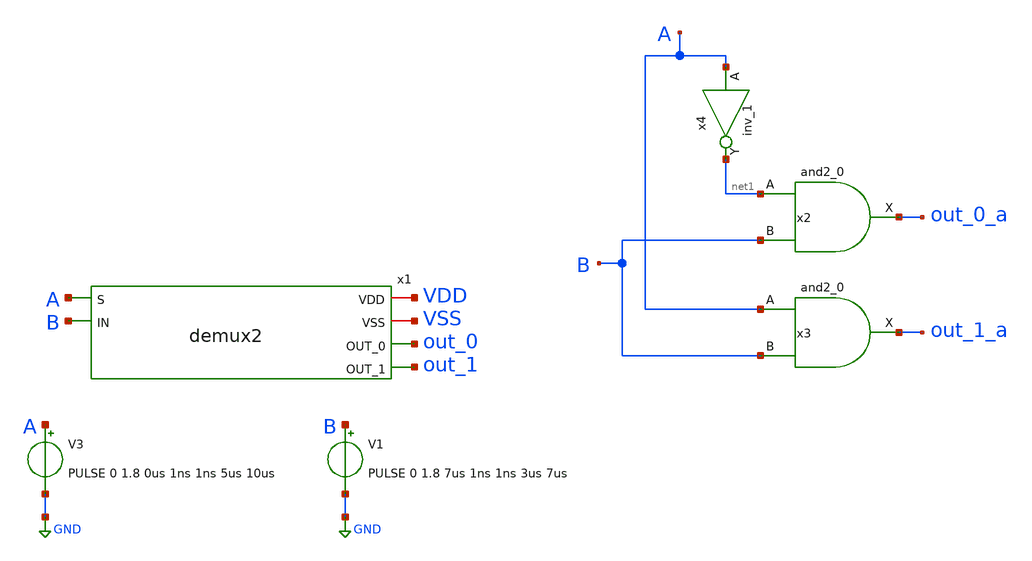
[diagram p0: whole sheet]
** sch_path: xschem/tests/dummy/dummy_test.sch
**.subckt dummy_test
V3 A GND PULSE 0 1.8 0us 1ns 1ns 5us 10us
V1 B GND PULSE 0 1.8 7us 1ns 1ns 3us 7us
x2 net1 B VSS VSS VDD VDD out_0_a sky130_fd_sc_hd__and2_0
x3 A B VSS VSS VDD VDD out_1_a sky130_fd_sc_hd__and2_0
x4 A VSS VSS VDD VDD net1 sky130_fd_sc_hd__inv_1
x1 A VDD VSS out_0 B out_1 demux2
**** begin user architecture code
 .lib $::SKYWATER_MODELS/sky130.lib.spice tt
.include $::SKYWATER_STDCELLS/sky130_fd_sc_hd.spice


.options acct list
.temp 25
vvcc VDD 0 dc 1.8
vvss VSS 0 0
.control
tran 0.1u 100u
* plot a b+2 clk+4 reset_b+6 x+8 y+10 q+12 qlatch+14
plot A B+2 out_0+4 out_1+6 out_0_a+8 out_1_a+10
write dummy_test.raw
.endc


**** end user architecture code
**.ends

* expanding   symbol:  src/demux2/demux2.sym # of pins=6
** sym_path: xschem/src/demux2/demux2.sym
** sch_path: xschem/src/demux2/demux2.sch
.subckt demux2 S VDD VSS OUT_0 IN OUT_1
*.ipin S
*.opin OUT_0
*.ipin IN
*.opin OUT_1
*.iopin VDD
*.iopin VSS
x1 net1 IN VSS VSS VDD VDD OUT_0 sky130_fd_sc_hd__and2_0
x2 S IN VSS VSS VDD VDD OUT_1 sky130_fd_sc_hd__and2_0
x3 S VSS VSS VDD VDD net1 sky130_fd_sc_hd__inv_1
.ends

.GLOBAL GND
.end
